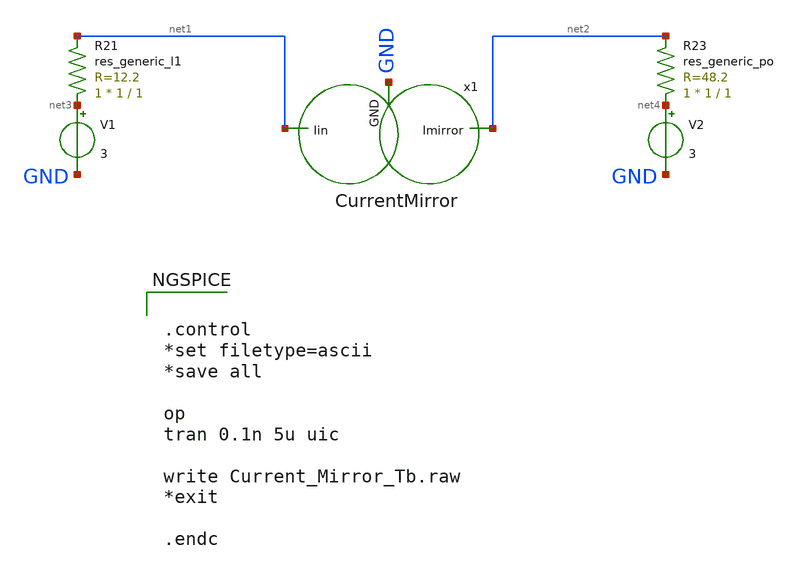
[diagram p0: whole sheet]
** sch_path: Current_Mirror_Tb.sch
**.subckt Current_Mirror_Tb
x1 GND net1 net2 CurrentMirror
V1 net3 GND 3
R21 net3 net1 sky130_fd_pr__res_generic_l1 W=1 L=1 m=1
V2 net4 GND 3
XR23 net4 net2 sky130_fd_pr__res_generic_po W=1 L=1 m=1
**** begin user architecture code

** opencircuitdesign pdks install
.lib $::SKYWATER_MODELS/sky130.lib.spice tt




.control
*set filetype=ascii
*save all

op
tran 0.1n 5u uic

write Current_Mirror_Tb.raw
*exit

.endc


**** end user architecture code
**.ends
.end
